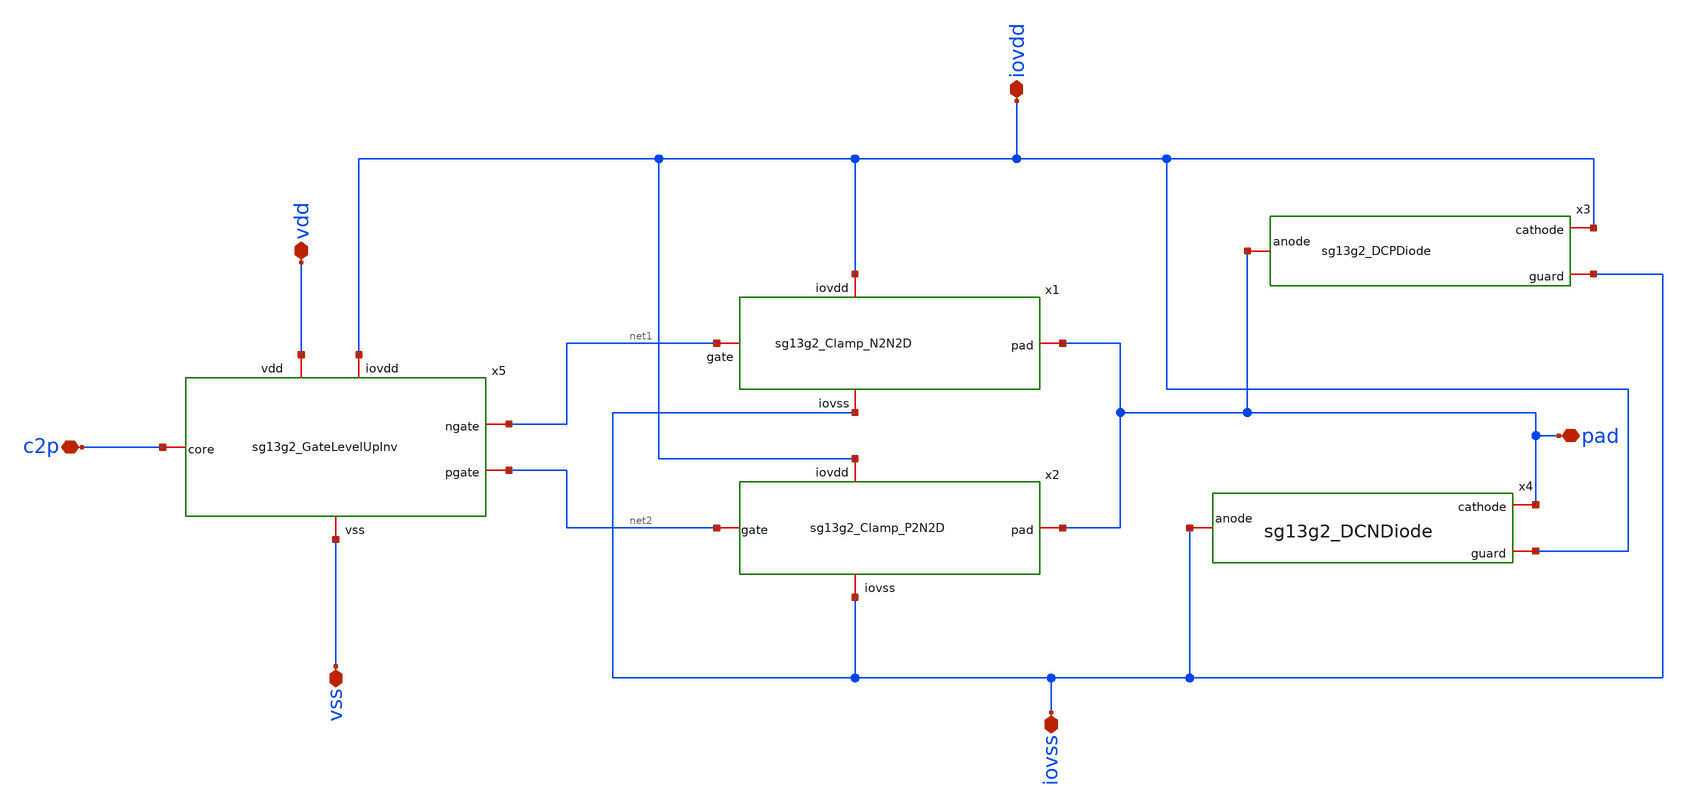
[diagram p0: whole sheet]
** sch_path: CDR4176-main/schematic/xschem/project_io/sg13g2_IOPadOut4mA/sg13g2_IOPadOut4mA.sch
**.subckt sg13g2_IOPadOut4mA vdd vss iovss iovdd c2p pad
*.iopin vdd
*.iopin vss
*.iopin iovss
*.iopin iovdd
*.iopin c2p
*.iopin pad
x1 iovdd pad net1 iovss sg13g2_Clamp_N2N2D
x2 iovdd net2 iovss pad sg13g2_Clamp_P2N2D
x5 vdd iovdd net1 net2 c2p vss sg13g2_GateLevelUpInv
x3 iovdd pad iovss sg13g2_DCPDiode
x4 pad iovss iovdd sg13g2_DCNDiode
**.ends
.end
